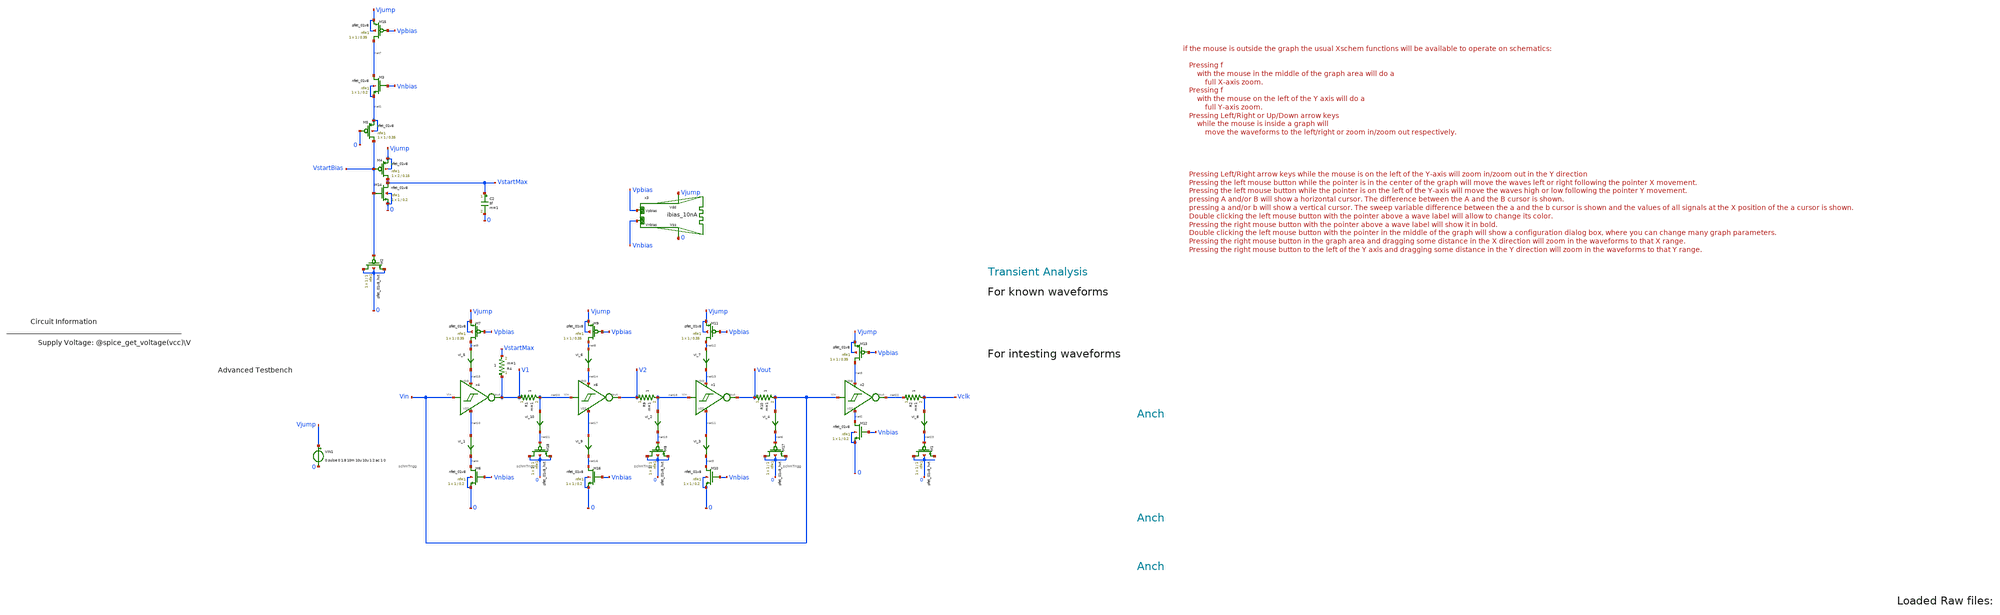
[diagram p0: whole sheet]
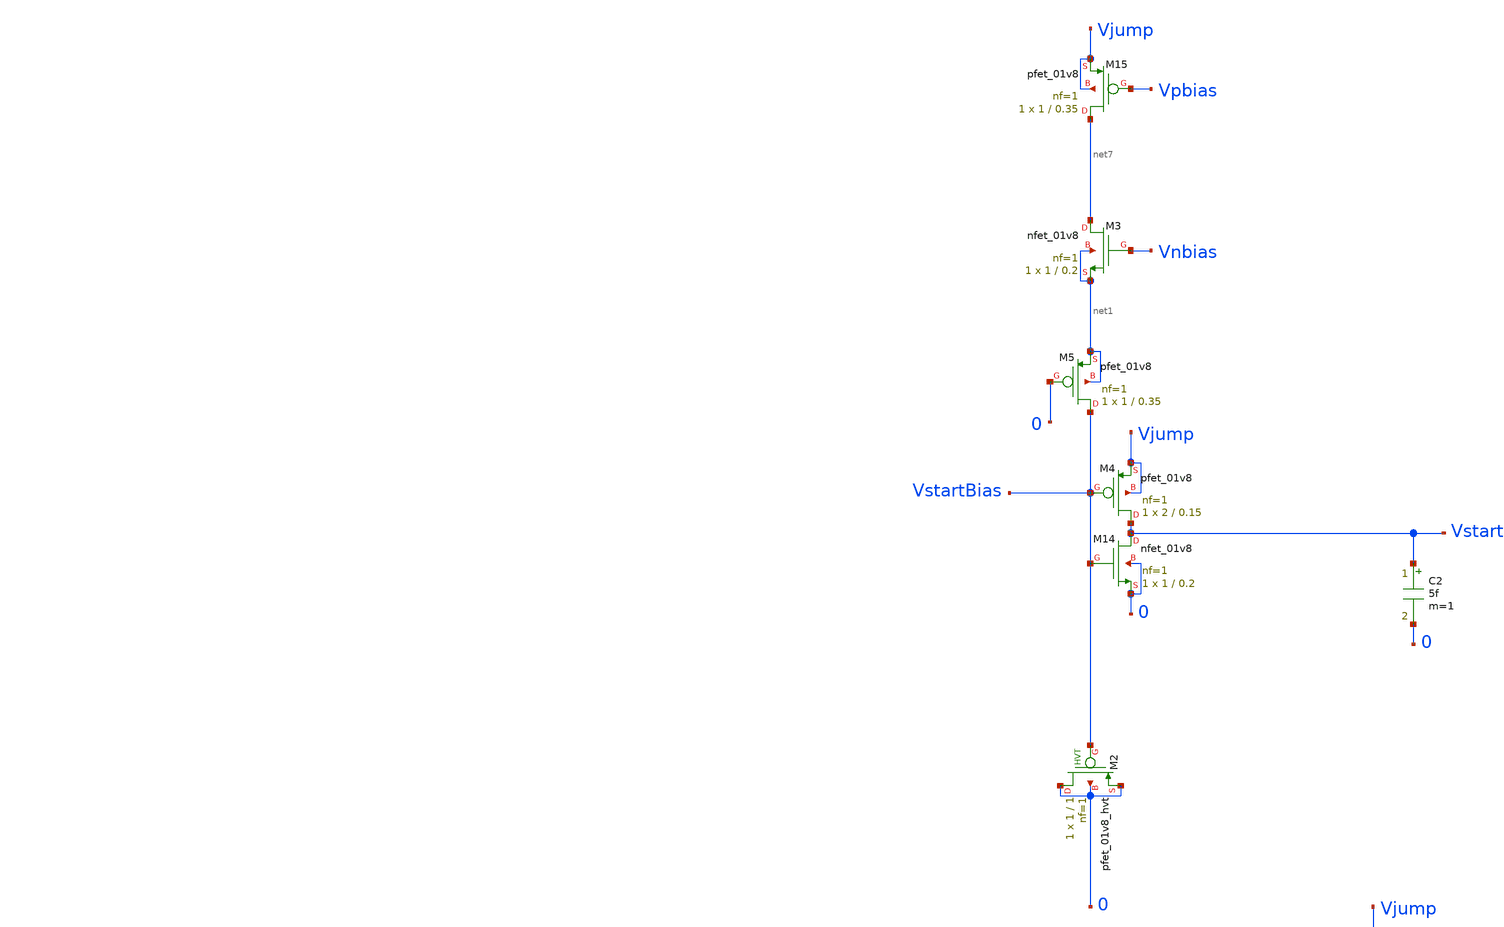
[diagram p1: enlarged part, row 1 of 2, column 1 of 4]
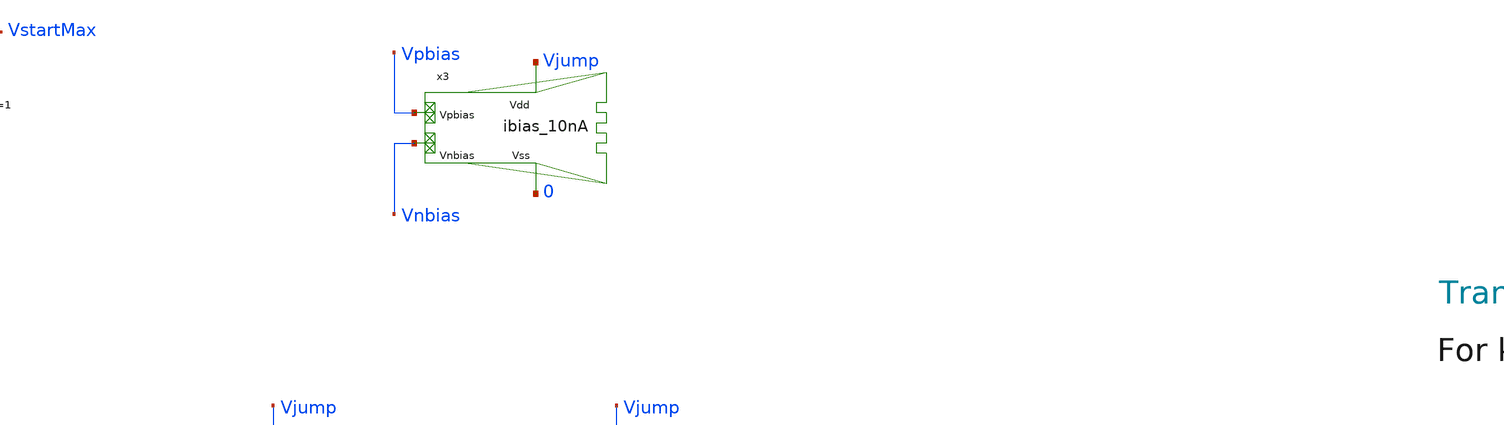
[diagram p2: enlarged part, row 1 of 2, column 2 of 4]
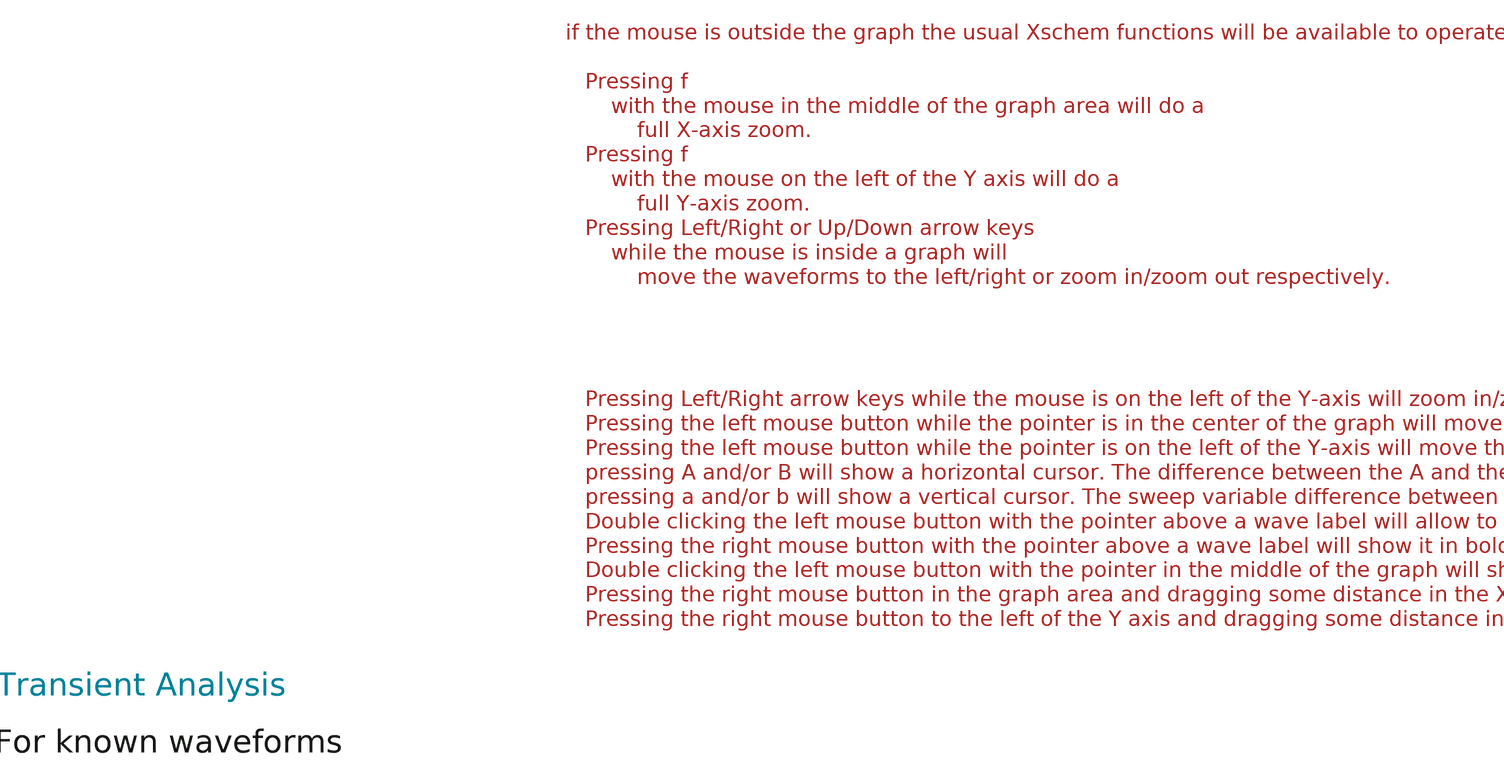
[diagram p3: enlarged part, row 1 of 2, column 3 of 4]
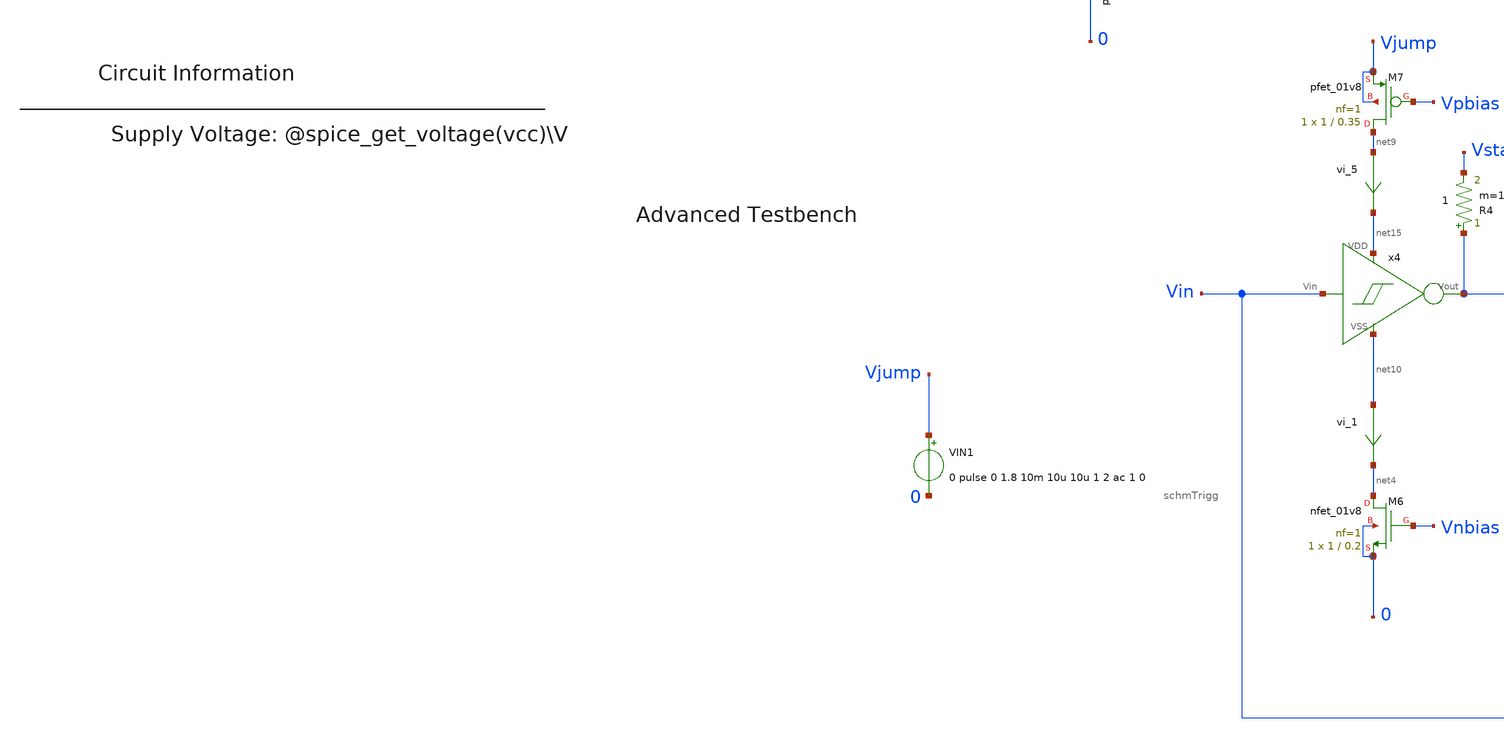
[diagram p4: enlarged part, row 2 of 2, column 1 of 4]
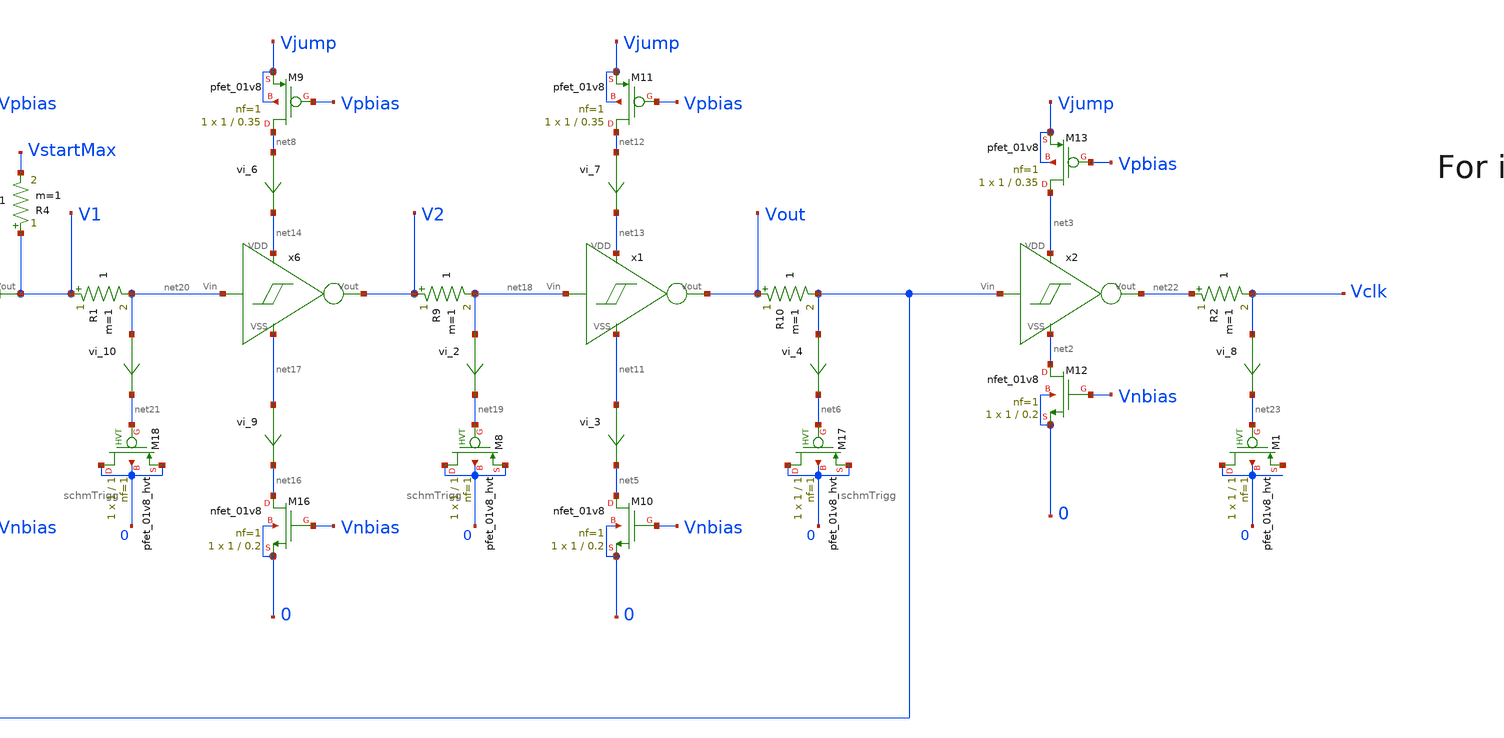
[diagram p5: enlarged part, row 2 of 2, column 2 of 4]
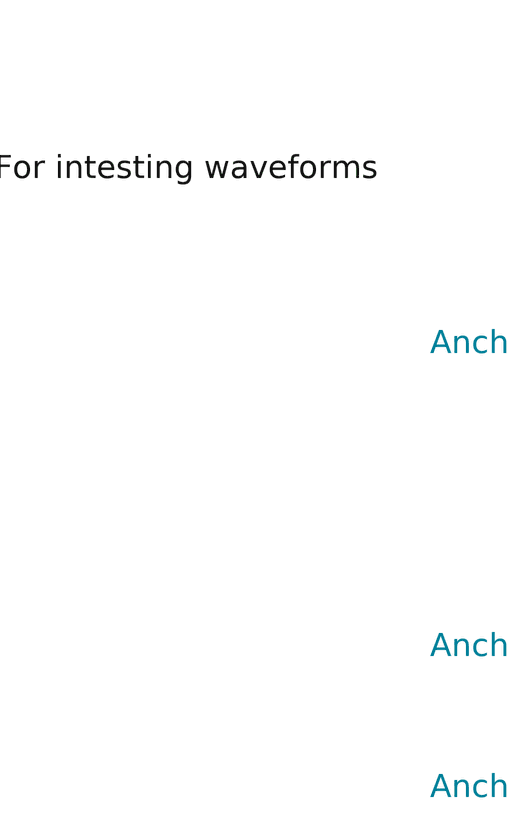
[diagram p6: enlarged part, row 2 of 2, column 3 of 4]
** sch_path: xschem/T3/oscillators/A_tt10_Ring_currentStarved/osc_schmTr_tran_tb.sch
* Copyright (C) 1998-2024 Stefan Frederik Schippers
* This program is free software; you can redistribute it and/or modify
* it under the terms of the GNU General Public License as published by
* the Free Software Foundation; either version 2 of the License, or
* (at your option) any later version.
* This program is distributed in the hope that it will be useful,
* but WITHOUT ANY WARRANTY; without even the implied warranty of
* MERCHANTABILITY or FITNESS FOR A PARTICULAR PURPOSE.  See the
* GNU General Public License for more details.
* You should have received a copy of the GNU General Public License
* along with this program; if not, write to the Free Software
**.subckt osc_schmTr_tran_tb
VIN1 Vjump 0 0 pulse 0 1.8 10m 10u 10u 1 2 ac 1 0
R9 V2 net18 1 m=1
XM4 VstartMax VstartBias Vjump Vjump sky130_fd_pr__pfet_01v8 L=0.15 W=2 nf=1 ad='int((nf+1)/2) * W/nf * 0.29'
+ as='int((nf+2)/2) * W/nf * 0.29' pd='2*int((nf+1)/2) * (W/nf + 0.29)' ps='2*int((nf+2)/2) * (W/nf + 0.29)'
+ nrd='0.29 / W' nrs='0.29 / W' sa=0 sb=0 sd=0 mult=1 m=1
XM5 VstartBias 0 net1 net1 sky130_fd_pr__pfet_01v8 L=0.35 W=1 nf=1 ad='int((nf+1)/2) * W/nf * 0.29' as='int((nf+2)/2) * W/nf * 0.29'
+ pd='2*int((nf+1)/2) * (W/nf + 0.29)' ps='2*int((nf+2)/2) * (W/nf + 0.29)' nrd='0.29 / W' nrs='0.29 / W'
+ sa=0 sb=0 sd=0 mult=1 m=1
XM2 0 VstartBias 0 0 sky130_fd_pr__pfet_01v8_hvt L=1 W=1 nf=1 ad='int((1 + 1)/2) * 1 / 1 * 0.29' as='int((1 + 2)/2) * 1 / 1 * 0.29'
+ pd='2*int((1 + 1)/2) * (1 / 1 + 0.29)' ps='2*int((1 + 2)/2) * (1 / 1 + 0.29)' nrd='0.29 / 1 ' nrs='0.29 / 1 '
+ sa=0 sb=0 sd=0 mult=1 m=1
x2 Vin net2 net3 net22 schmTrigg
x3 Vjump 0 Vnbias Vpbias ibias_10nA
XM6 net4 Vnbias 0 0 sky130_fd_pr__nfet_01v8 L=0.2 W=1 nf=1 ad='int((1 + 1)/2) * 1 / 1 * 0.29' as='int((1 + 2)/2) * 1 / 1 * 0.29'
+ pd='2*int((1 + 1)/2) * (1 / 1 + 0.29)' ps='2*int((1 + 2)/2) * (1 / 1 + 0.29)' nrd='0.29 / 1 ' nrs='0.29 / 1 '
+ sa=0 sb=0 sd=0 mult=1 m=1
XM7 net9 Vpbias Vjump Vjump sky130_fd_pr__pfet_01v8 L=0.35 W=1 nf=1 ad='int((nf+1)/2) * W/nf * 0.29'
+ as='int((nf+2)/2) * W/nf * 0.29' pd='2*int((nf+1)/2) * (W/nf + 0.29)' ps='2*int((nf+2)/2) * (W/nf + 0.29)'
+ nrd='0.29 / W' nrs='0.29 / W' sa=0 sb=0 sd=0 mult=1 m=1
XM9 net8 Vpbias Vjump Vjump sky130_fd_pr__pfet_01v8 L=0.35 W=1 nf=1 ad='int((nf+1)/2) * W/nf * 0.29'
+ as='int((nf+2)/2) * W/nf * 0.29' pd='2*int((nf+1)/2) * (W/nf + 0.29)' ps='2*int((nf+2)/2) * (W/nf + 0.29)'
+ nrd='0.29 / W' nrs='0.29 / W' sa=0 sb=0 sd=0 mult=1 m=1
XM10 net5 Vnbias 0 0 sky130_fd_pr__nfet_01v8 L=0.2 W=1 nf=1 ad='int((1 + 1)/2) * 1 / 1 * 0.29' as='int((1 + 2)/2) * 1 / 1 * 0.29'
+ pd='2*int((1 + 1)/2) * (1 / 1 + 0.29)' ps='2*int((1 + 2)/2) * (1 / 1 + 0.29)' nrd='0.29 / 1 ' nrs='0.29 / 1 '
+ sa=0 sb=0 sd=0 mult=1 m=1
XM11 net12 Vpbias Vjump Vjump sky130_fd_pr__pfet_01v8 L=0.35 W=1 nf=1 ad='int((nf+1)/2) * W/nf * 0.29'
+ as='int((nf+2)/2) * W/nf * 0.29' pd='2*int((nf+1)/2) * (W/nf + 0.29)' ps='2*int((nf+2)/2) * (W/nf + 0.29)'
+ nrd='0.29 / W' nrs='0.29 / W' sa=0 sb=0 sd=0 mult=1 m=1
XM12 net2 Vnbias 0 0 sky130_fd_pr__nfet_01v8 L=0.2 W=1 nf=1 ad='int((1 + 1)/2) * 1 / 1 * 0.29' as='int((1 + 2)/2) * 1 / 1 * 0.29'
+ pd='2*int((1 + 1)/2) * (1 / 1 + 0.29)' ps='2*int((1 + 2)/2) * (1 / 1 + 0.29)' nrd='0.29 / 1 ' nrs='0.29 / 1 '
+ sa=0 sb=0 sd=0 mult=1 m=1
XM13 net3 Vpbias Vjump Vjump sky130_fd_pr__pfet_01v8 L=0.35 W=1 nf=1 ad='int((nf+1)/2) * W/nf * 0.29'
+ as='int((nf+2)/2) * W/nf * 0.29' pd='2*int((nf+1)/2) * (W/nf + 0.29)' ps='2*int((nf+2)/2) * (W/nf + 0.29)'
+ nrd='0.29 / W' nrs='0.29 / W' sa=0 sb=0 sd=0 mult=1 m=1
XM15 net7 Vpbias Vjump Vjump sky130_fd_pr__pfet_01v8 L=0.35 W=1 nf=1 ad='int((nf+1)/2) * W/nf * 0.29'
+ as='int((nf+2)/2) * W/nf * 0.29' pd='2*int((nf+1)/2) * (W/nf + 0.29)' ps='2*int((nf+2)/2) * (W/nf + 0.29)'
+ nrd='0.29 / W' nrs='0.29 / W' sa=0 sb=0 sd=0 mult=1 m=1
vi_1 net10 net4 0
.save i(vi_1)
C2 VstartMax 0 5f m=1
R4 V1 VstartMax 1 m=1
R10 Vout Vin 1 m=1
XM17 0 net6 0 0 sky130_fd_pr__pfet_01v8_hvt L=1 W=1 nf=1 ad='int((1 + 1)/2) * 1 / 1 * 0.29' as='int((1 + 2)/2) * 1 / 1 * 0.29'
+ pd='2*int((1 + 1)/2) * (1 / 1 + 0.29)' ps='2*int((1 + 2)/2) * (1 / 1 + 0.29)' nrd='0.29 / 1 ' nrs='0.29 / 1 '
+ sa=0 sb=0 sd=0 mult=1 m=1
vi_3 net11 net5 0
.save i(vi_3)
vi_4 Vin net6 0
.save i(vi_4)
vi_5 net9 net15 0
.save i(vi_5)
vi_6 net8 net14 0
.save i(vi_6)
vi_7 net12 net13 0
.save i(vi_7)
XM3 net7 Vnbias net1 net1 sky130_fd_pr__nfet_01v8 L=0.2 W=1 nf=1 ad='int((1 + 1)/2) * 1 / 1 * 0.29' as='int((1 + 2)/2) * 1 / 1 * 0.29'
+ pd='2*int((1 + 1)/2) * (1 / 1 + 0.29)' ps='2*int((1 + 2)/2) * (1 / 1 + 0.29)' nrd='0.29 / 1 ' nrs='0.29 / 1 '
+ sa=0 sb=0 sd=0 mult=1 m=1
XM14 VstartMax VstartBias 0 0 sky130_fd_pr__nfet_01v8 L=0.2 W=1 nf=1 ad='int((1 + 1)/2) * 1 / 1 * 0.29'
+ as='int((1 + 2)/2) * 1 / 1 * 0.29' pd='2*int((1 + 1)/2) * (1 / 1 + 0.29)' ps='2*int((1 + 2)/2) * (1 / 1 + 0.29)'
+ nrd='0.29 / 1 ' nrs='0.29 / 1 ' sa=0 sb=0 sd=0 mult=1 m=1
x6 net20 net17 net14 V2 schmTrigg
x1 net18 net11 net13 Vout schmTrigg
x4 Vin net10 net15 V1 schmTrigg
XM16 net16 Vnbias 0 0 sky130_fd_pr__nfet_01v8 L=0.2 W=1 nf=1 ad='int((1 + 1)/2) * 1 / 1 * 0.29' as='int((1 + 2)/2) * 1 / 1 * 0.29'
+ pd='2*int((1 + 1)/2) * (1 / 1 + 0.29)' ps='2*int((1 + 2)/2) * (1 / 1 + 0.29)' nrd='0.29 / 1 ' nrs='0.29 / 1 '
+ sa=0 sb=0 sd=0 mult=1 m=1
vi_9 net17 net16 0
.save i(vi_9)
XM8 0 net19 0 0 sky130_fd_pr__pfet_01v8_hvt L=1 W=1 nf=1 ad='int((1 + 1)/2) * 1 / 1 * 0.29' as='int((1 + 2)/2) * 1 / 1 * 0.29'
+ pd='2*int((1 + 1)/2) * (1 / 1 + 0.29)' ps='2*int((1 + 2)/2) * (1 / 1 + 0.29)' nrd='0.29 / 1 ' nrs='0.29 / 1 '
+ sa=0 sb=0 sd=0 mult=1 m=1
vi_2 net18 net19 0
.save i(vi_2)
R1 V1 net20 1 m=1
XM18 0 net21 0 0 sky130_fd_pr__pfet_01v8_hvt L=1 W=1 nf=1 ad='int((1 + 1)/2) * 1 / 1 * 0.29' as='int((1 + 2)/2) * 1 / 1 * 0.29'
+ pd='2*int((1 + 1)/2) * (1 / 1 + 0.29)' ps='2*int((1 + 2)/2) * (1 / 1 + 0.29)' nrd='0.29 / 1 ' nrs='0.29 / 1 '
+ sa=0 sb=0 sd=0 mult=1 m=1
vi_10 net20 net21 0
.save i(vi_10)
R2 net22 Vclk 1 m=1
XM1 0 net23 net24 0 sky130_fd_pr__pfet_01v8_hvt L=1 W=1 nf=1 ad='int((1 + 1)/2) * 1 / 1 * 0.29' as='int((1 + 2)/2) * 1 / 1 * 0.29'
+ pd='2*int((1 + 1)/2) * (1 / 1 + 0.29)' ps='2*int((1 + 2)/2) * (1 / 1 + 0.29)' nrd='0.29 / 1 ' nrs='0.29 / 1 '
+ sa=0 sb=0 sd=0 mult=1 m=1
vi_8 Vclk net23 0
.save i(vi_8)
**** begin user architecture code



.temp 30
.param Vdd = 1.8
.param imax = 600e-9
.param var_cap = 1p
.param var_res = 7000k


.option savecurrents
.save all @m14[gm]
.control
  save all alli
  save @m.xm14.msky130_fd_pr__nfet_01v8[gm]

  op
  let power=-v(vcc) * i(vvcc)
  settype power power
  write template_adv_tb.raw
  set appendwrite


  tran 100u 300m
  write template_adv_tb.raw





  quit 0




.endc





** opencircuitdesign pdks install
.lib $::SKYWATER_MODELS/sky130.lib.spice tt


**** end user architecture code
**.ends

* expanding   symbol:  T1/schmTrigg/schmTrigg.sym # of pins=4
** sym_path: xschem/T1/schmTrigg/schmTrigg.sym
** sch_path: xschem/T1/schmTrigg/schmTrigg.sch
.subckt schmTrigg Vin VSS VDD Vout
*.ipin Vin
*.ipin VDD
*.ipin VSS
*.opin Vout
XM1 VDD Vout Vn Vn sky130_fd_pr__nfet_01v8 L=0.15 W=1 nf=1 ad='int((1 + 1)/2) * 1 / 1 * 0.29' as='int((1 + 2)/2) * 1 / 1 * 0.29'
+ pd='2*int((1 + 1)/2) * (1 / 1 + 0.29)' ps='2*int((1 + 2)/2) * (1 / 1 + 0.29)' nrd='0.29 / 1 ' nrs='0.29 / 1 '
+ sa=0 sb=0 sd=0 mult=1 m=1
XM2 Vn Vin VSS VSS sky130_fd_pr__nfet_01v8 L=0.15 W=1 nf=1 ad='int((1 + 1)/2) * 1 / 1 * 0.29' as='int((1 + 2)/2) * 1 / 1 * 0.29'
+ pd='2*int((1 + 1)/2) * (1 / 1 + 0.29)' ps='2*int((1 + 2)/2) * (1 / 1 + 0.29)' nrd='0.29 / 1 ' nrs='0.29 / 1 '
+ sa=0 sb=0 sd=0 mult=1 m=1
XM3 Vout Vin Vn Vn sky130_fd_pr__nfet_01v8 L=0.15 W=1 nf=1 ad='int((1 + 1)/2) * 1 / 1 * 0.29' as='int((1 + 2)/2) * 1 / 1 * 0.29'
+ pd='2*int((1 + 1)/2) * (1 / 1 + 0.29)' ps='2*int((1 + 2)/2) * (1 / 1 + 0.29)' nrd='0.29 / 1 ' nrs='0.29 / 1 '
+ sa=0 sb=0 sd=0 mult=1 m=1
XM4 VSS Vout Vp Vp sky130_fd_pr__pfet_01v8 L=0.15 W=1 nf=1 ad='int((nf+1)/2) * W/nf * 0.29' as='int((nf+2)/2) * W/nf * 0.29'
+ pd='2*int((nf+1)/2) * (W/nf + 0.29)' ps='2*int((nf+2)/2) * (W/nf + 0.29)' nrd='0.29 / W' nrs='0.29 / W'
+ sa=0 sb=0 sd=0 mult=1 m=1
XM5 Vout Vin Vp Vp sky130_fd_pr__pfet_01v8 L=0.15 W=1 nf=1 ad='int((nf+1)/2) * W/nf * 0.29' as='int((nf+2)/2) * W/nf * 0.29'
+ pd='2*int((nf+1)/2) * (W/nf + 0.29)' ps='2*int((nf+2)/2) * (W/nf + 0.29)' nrd='0.29 / W' nrs='0.29 / W'
+ sa=0 sb=0 sd=0 mult=1 m=1
XM6 Vp Vin VDD VDD sky130_fd_pr__pfet_01v8 L=0.15 W=1 nf=1 ad='int((nf+1)/2) * W/nf * 0.29' as='int((nf+2)/2) * W/nf * 0.29'
+ pd='2*int((nf+1)/2) * (W/nf + 0.29)' ps='2*int((nf+2)/2) * (W/nf + 0.29)' nrd='0.29 / W' nrs='0.29 / W'
+ sa=0 sb=0 sd=0 mult=1 m=1
.ends


* expanding   symbol:  T2/biasGen/A_tt10_10nA/ibias_10nA.sym # of pins=4
** sym_path: T2/biasGen/A_tt10_10nA/ibias_10nA.sym
** sch_path: T2/biasGen/A_tt10_10nA/ibias_10nA.sch
.subckt ibias_10nA Vdd Vss Vnbias Vpbias
*.ipin Vdd
*.ipin Vss
*.opin Vnbias
*.opin Vpbias
XM56 Vpbias Vpbias Vdd Vdd sky130_fd_pr__pfet_01v8 L=0.35 W=1 nf=1 ad='int((nf+1)/2) * W/nf * 0.29' as='int((nf+2)/2) * W/nf * 0.29'
+ pd='2*int((nf+1)/2) * (W/nf + 0.29)' ps='2*int((nf+2)/2) * (W/nf + 0.29)' nrd='0.29 / W' nrs='0.29 / W'
+ sa=0 sb=0 sd=0 mult=1 m=1
XM57 Vnbias Vpbias Vdd Vdd sky130_fd_pr__pfet_01v8 L=0.35 W=1 nf=1 ad='int((nf+1)/2) * W/nf * 0.29' as='int((nf+2)/2) * W/nf * 0.29'
+ pd='2*int((nf+1)/2) * (W/nf + 0.29)' ps='2*int((nf+2)/2) * (W/nf + 0.29)' nrd='0.29 / W' nrs='0.29 / W'
+ sa=0 sb=0 sd=0 mult=1 m=1
XM58 net2 Vpbias Vdd Vdd sky130_fd_pr__pfet_01v8 L=0.30 W=2 nf=1 ad='int((nf+1)/2) * W/nf * 0.29' as='int((nf+2)/2) * W/nf * 0.29'
+ pd='2*int((nf+1)/2) * (W/nf + 0.29)' ps='2*int((nf+2)/2) * (W/nf + 0.29)' nrd='0.29 / W' nrs='0.29 / W'
+ sa=0 sb=0 sd=0 mult=1 m=1
XM59 Vpbias Vnbias net1 net1 sky130_fd_pr__nfet_01v8 L=0.2 W=1 nf=1 ad='int((1 + 1)/2) * 1 / 1 * 0.29'
+ as='int((1 + 2)/2) * 1 / 1 * 0.29' pd='2*int((1 + 1)/2) * (1 / 1 + 0.29)' ps='2*int((1 + 2)/2) * (1 / 1 + 0.29)'
+ nrd='0.29 / 1 ' nrs='0.29 / 1 ' sa=0 sb=0 sd=0 mult=1 m=1
XM60 Vnbias Vnbias Vss Vss sky130_fd_pr__nfet_01v8 L=0.2 W=1 nf=1 ad='int((1 + 1)/2) * 1 / 1 * 0.29'
+ as='int((1 + 2)/2) * 1 / 1 * 0.29' pd='2*int((1 + 1)/2) * (1 / 1 + 0.29)' ps='2*int((1 + 2)/2) * (1 / 1 + 0.29)'
+ nrd='0.29 / 1 ' nrs='0.29 / 1 ' sa=0 sb=0 sd=0 mult=1 m=1
XM61 net2 net2 net1 net1 sky130_fd_pr__nfet_01v8 L=0.2 W=1 nf=1 ad='int((1 + 1)/2) * 1 / 1 * 0.29' as='int((1 + 2)/2) * 1 / 1 * 0.29'
+ pd='2*int((1 + 1)/2) * (1 / 1 + 0.29)' ps='2*int((1 + 2)/2) * (1 / 1 + 0.29)' nrd='0.29 / 1 ' nrs='0.29 / 1 '
+ sa=0 sb=0 sd=0 mult=1 m=1
XM62 net1 net2 Vss Vss sky130_fd_pr__nfet_01v8 L=1 W=1 nf=1 ad='int((1 + 1)/2) * 1 / 1 * 0.29' as='int((1 + 2)/2) * 1 / 1 * 0.29'
+ pd='2*int((1 + 1)/2) * (1 / 1 + 0.29)' ps='2*int((1 + 2)/2) * (1 / 1 + 0.29)' nrd='0.29 / 1 ' nrs='0.29 / 1 '
+ sa=0 sb=0 sd=0 mult=1 m=1
.ends

.end
